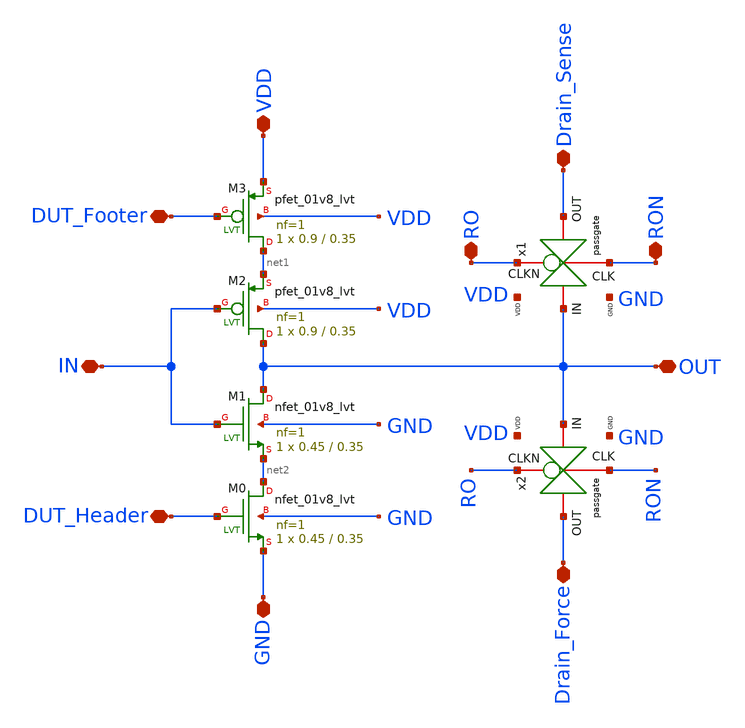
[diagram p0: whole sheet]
** sch_path: LVT/rovcel1_LVT/rovcel1_LVT.sch
**.subckt rovcel1_LVT OUT Drain_Force DUT_Footer DUT_Header IN Drain_Sense VDD GND RO RON
*.iopin OUT
*.iopin Drain_Force
*.iopin DUT_Footer
*.iopin DUT_Header
*.iopin IN
*.iopin Drain_Sense
*.iopin VDD
*.iopin GND
*.iopin RO
*.iopin RON
XM0 net2 DUT_Header GND GND sky130_fd_pr__nfet_01v8_lvt L=0.35 W=0.45 nf=1 ad='int((nf+1)/2) * W/nf * 0.29'
+ as='int((nf+2)/2) * W/nf * 0.29' pd='2*int((nf+1)/2) * (W/nf + 0.29)' ps='2*int((nf+2)/2) * (W/nf + 0.29)'
+ nrd='0.29 / W' nrs='0.29 / W' sa=0 sb=0 sd=0 mult=1 m=1
XM1 OUT IN net2 GND sky130_fd_pr__nfet_01v8_lvt L=0.35 W=0.45 nf=1 ad='int((nf+1)/2) * W/nf * 0.29' as='int((nf+2)/2) * W/nf * 0.29'
+ pd='2*int((nf+1)/2) * (W/nf + 0.29)' ps='2*int((nf+2)/2) * (W/nf + 0.29)' nrd='0.29 / W' nrs='0.29 / W'
+ sa=0 sb=0 sd=0 mult=1 m=1
XM2 OUT IN net1 VDD sky130_fd_pr__pfet_01v8_lvt L=0.35 W=0.9 nf=1 ad='int((nf+1)/2) * W/nf * 0.29' as='int((nf+2)/2) * W/nf * 0.29'
+ pd='2*int((nf+1)/2) * (W/nf + 0.29)' ps='2*int((nf+2)/2) * (W/nf + 0.29)' nrd='0.29 / W' nrs='0.29 / W'
+ sa=0 sb=0 sd=0 mult=1 m=1
XM3 net1 DUT_Footer VDD VDD sky130_fd_pr__pfet_01v8_lvt L=0.35 W=0.9 nf=1 ad='int((nf+1)/2) * W/nf * 0.29'
+ as='int((nf+2)/2) * W/nf * 0.29' pd='2*int((nf+1)/2) * (W/nf + 0.29)' ps='2*int((nf+2)/2) * (W/nf + 0.29)'
+ nrd='0.29 / W' nrs='0.29 / W' sa=0 sb=0 sd=0 mult=1 m=1
x1 RO OUT Drain_Sense RON GND VDD passgate
x2 RO OUT Drain_Force RON GND VDD passgate
**.ends
.end
